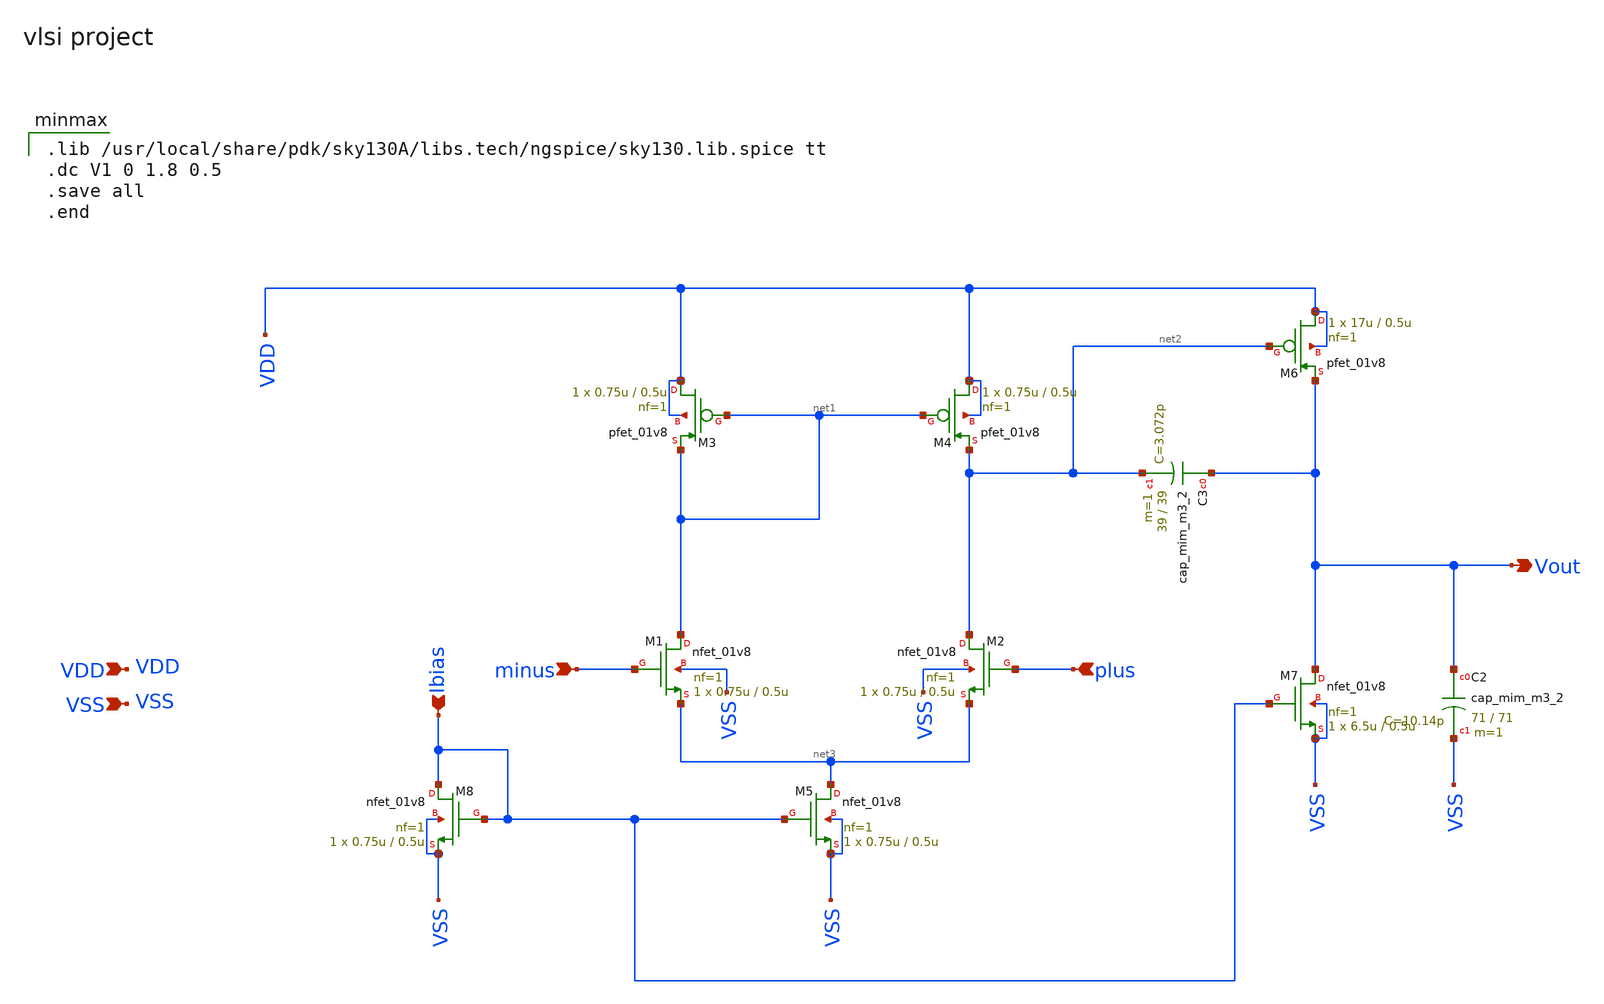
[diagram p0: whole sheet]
** sch_path: xschem/2stageopamp.sch
**.subckt 2stageopamp minus plus Vout VDD VSS Ibias
*.ipin minus
*.ipin plus
*.opin Vout
*.ipin VDD
*.ipin VSS
*.ipin Ibias
XM1 net1 minus net3 VSS sky130_fd_pr__nfet_01v8 L=0.5u W=0.75u nf=1 ad='int((nf+1)/2) * W/nf * 0.29'
+ as='int((nf+2)/2) * W/nf * 0.29' pd='2*int((nf+1)/2) * (W/nf + 0.29)' ps='2*int((nf+2)/2) * (W/nf + 0.29)'
+ nrd='0.29 / W' nrs='0.29 / W' sa=0 sb=0 sd=0 mult=1 m=1
XM2 net2 plus net3 VSS sky130_fd_pr__nfet_01v8 L=0.5u W=0.75u nf=1 ad='int((nf+1)/2) * W/nf * 0.29' as='int((nf+2)/2) * W/nf * 0.29'
+ pd='2*int((nf+1)/2) * (W/nf + 0.29)' ps='2*int((nf+2)/2) * (W/nf + 0.29)' nrd='0.29 / W' nrs='0.29 / W'
+ sa=0 sb=0 sd=0 mult=1 m=1
XM5 net3 Ibias VSS VSS sky130_fd_pr__nfet_01v8 L=0.5u W=0.75u nf=1 ad='int((nf+1)/2) * W/nf * 0.29' as='int((nf+2)/2) * W/nf * 0.29'
+ pd='2*int((nf+1)/2) * (W/nf + 0.29)' ps='2*int((nf+2)/2) * (W/nf + 0.29)' nrd='0.29 / W' nrs='0.29 / W'
+ sa=0 sb=0 sd=0 mult=1 m=1
XM7 Vout Ibias VSS VSS sky130_fd_pr__nfet_01v8 L=0.5u W=6.5u nf=1 ad='int((nf+1)/2) * W/nf * 0.29' as='int((nf+2)/2) * W/nf * 0.29'
+ pd='2*int((nf+1)/2) * (W/nf + 0.29)' ps='2*int((nf+2)/2) * (W/nf + 0.29)' nrd='0.29 / W' nrs='0.29 / W'
+ sa=0 sb=0 sd=0 mult=1 m=1
XM8 Ibias Ibias VSS VSS sky130_fd_pr__nfet_01v8 L=0.5u W=0.75u nf=1 ad='int((nf+1)/2) * W/nf * 0.29'
+ as='int((nf+2)/2) * W/nf * 0.29' pd='2*int((nf+1)/2) * (W/nf + 0.29)' ps='2*int((nf+2)/2) * (W/nf + 0.29)'
+ nrd='0.29 / W' nrs='0.29 / W' sa=0 sb=0 sd=0 mult=1 m=1
XM4 VDD net1 net2 VDD sky130_fd_pr__pfet_01v8 L=0.5u W=0.75u nf=1 ad='int((nf+1)/2) * W/nf * 0.29' as='int((nf+2)/2) * W/nf * 0.29'
+ pd='2*int((nf+1)/2) * (W/nf + 0.29)' ps='2*int((nf+2)/2) * (W/nf + 0.29)' nrd='0.29 / W' nrs='0.29 / W'
+ sa=0 sb=0 sd=0 mult=1 m=1
XM3 VDD net1 net1 VDD sky130_fd_pr__pfet_01v8 L=0.5u W=0.75u nf=1 ad='int((nf+1)/2) * W/nf * 0.29' as='int((nf+2)/2) * W/nf * 0.29'
+ pd='2*int((nf+1)/2) * (W/nf + 0.29)' ps='2*int((nf+2)/2) * (W/nf + 0.29)' nrd='0.29 / W' nrs='0.29 / W'
+ sa=0 sb=0 sd=0 mult=1 m=1
XM6 VDD net2 Vout VDD sky130_fd_pr__pfet_01v8 L=0.5u W=17u nf=1 ad='int((nf+1)/2) * W/nf * 0.29' as='int((nf+2)/2) * W/nf * 0.29'
+ pd='2*int((nf+1)/2) * (W/nf + 0.29)' ps='2*int((nf+2)/2) * (W/nf + 0.29)' nrd='0.29 / W' nrs='0.29 / W'
+ sa=0 sb=0 sd=0 mult=1 m=1
XC3 Vout net2 sky130_fd_pr__cap_mim_m3_2 W=39 L=39 MF=1 m=1
XC2 Vout VSS sky130_fd_pr__cap_mim_m3_2 W=71 L=71 MF=1 m=1
**** begin user architecture code

.lib /usr/local/share/pdk/sky130A/libs.tech/ngspice/sky130.lib.spice tt
.dc V1 0 1.8 0.5
.save all
.end

**** end user architecture code
**.ends
.end
